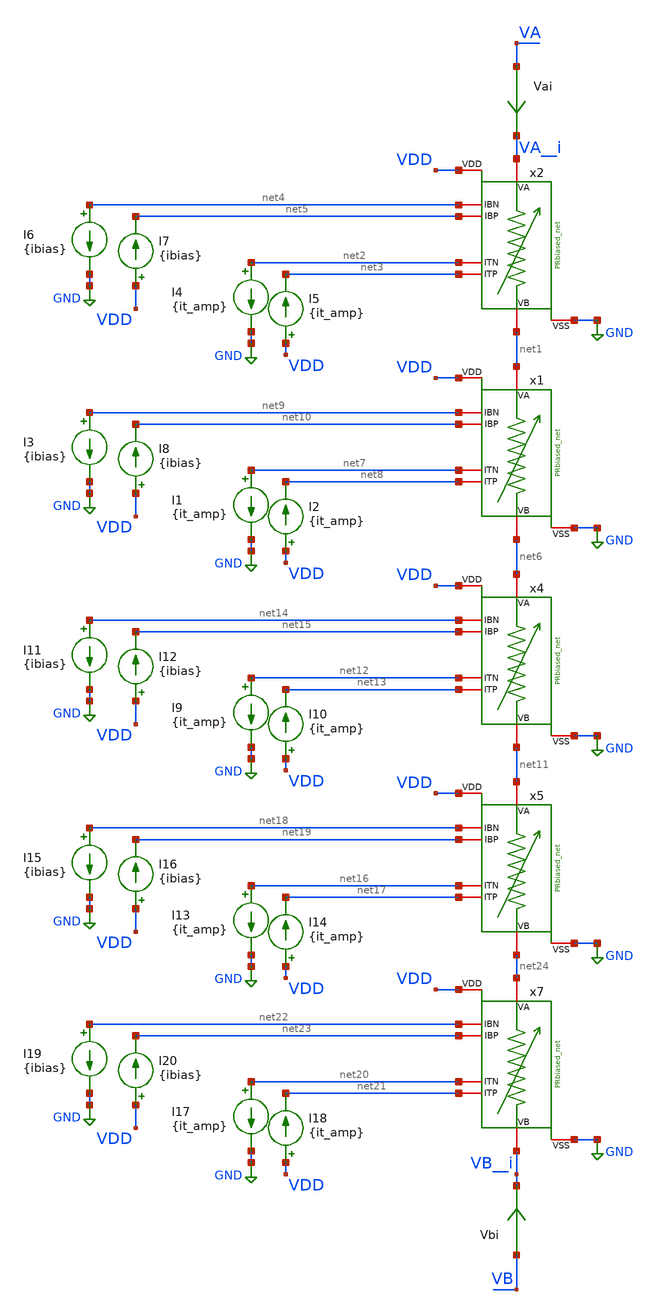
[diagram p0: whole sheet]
** sch_path: TIA_Filter/untitled.sch
**.subckt untitled
Vai VA VA__i 0
.save i(vai)
I4 net2 GND {it_amp}
I5 VDD net3 {it_amp}
I6 net4 GND {ibias}
I7 VDD net5 {ibias}
x1 net1 net6 net9 net10 net7 net8 VDD GND PRbiased_net
I1 net7 GND {it_amp}
I2 VDD net8 {it_amp}
I3 net9 GND {ibias}
I8 VDD net10 {ibias}
x4 net6 net11 net14 net15 net12 net13 VDD GND PRbiased_net
I9 net12 GND {it_amp}
I10 VDD net13 {it_amp}
I11 net14 GND {ibias}
I12 VDD net15 {ibias}
x5 net11 net24 net18 net19 net16 net17 VDD GND PRbiased_net
I13 net16 GND {it_amp}
I14 VDD net17 {it_amp}
I15 net18 GND {ibias}
I16 VDD net19 {ibias}
x7 net24 VB__i net22 net23 net20 net21 VDD GND PRbiased_net
I17 net20 GND {it_amp}
I18 VDD net21 {it_amp}
I19 net22 GND {ibias}
I20 VDD net23 {ibias}
Vbi VB VB__i 0
.save i(vbi)
x2 VA__i net1 net4 net5 net2 net3 VDD GND PRbiased_net
**.ends
.GLOBAL GND
.end
